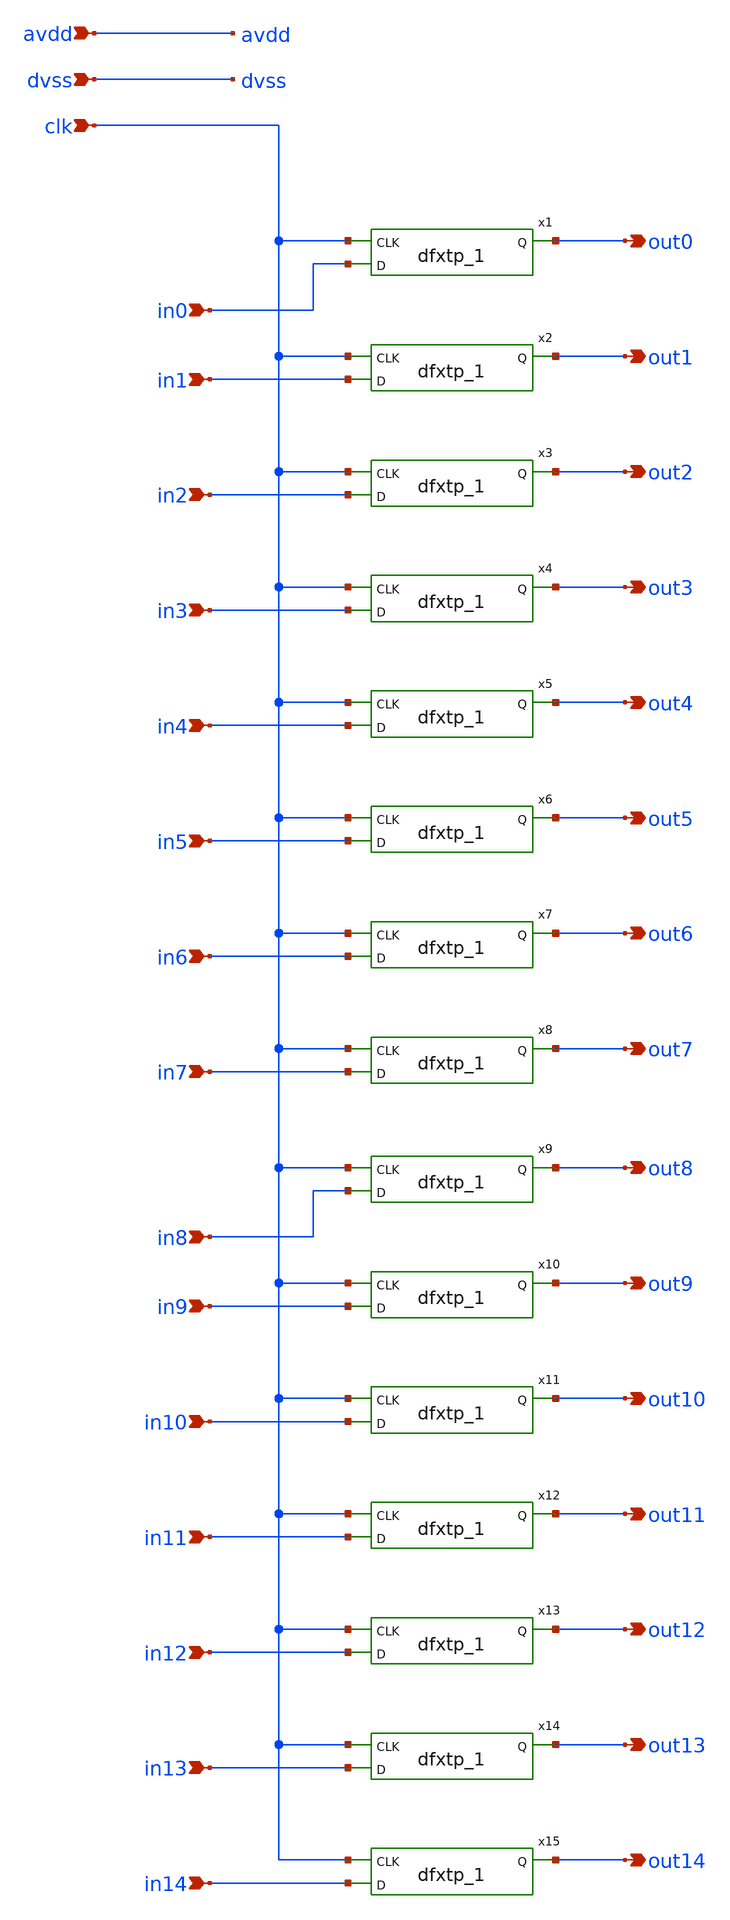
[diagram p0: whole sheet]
** sch_path: xschem/dff15ch.sch
**.subckt dff15ch out0 out1 out2 out3 out4 out5 out6 out7 in0 in1 in2 in3 in4 in5 in6 in7 out8 out9
*+ out10 out11 out12 out13 out14 in8 in9 in10 in11 in12 in13 in14 avdd dvss clk
*.opin out0
*.opin out1
*.opin out2
*.opin out3
*.opin out4
*.opin out5
*.opin out6
*.opin out7
*.ipin in0
*.ipin in1
*.ipin in2
*.ipin in3
*.ipin in4
*.ipin in5
*.ipin in6
*.ipin in7
*.opin out8
*.opin out9
*.opin out10
*.opin out11
*.opin out12
*.opin out13
*.opin out14
*.ipin in8
*.ipin in9
*.ipin in10
*.ipin in11
*.ipin in12
*.ipin in13
*.ipin in14
*.ipin avdd
*.ipin dvss
*.ipin clk
x1 clk in0 dvss dvss avdd avdd out0 sky130_fd_sc_hvl__dfxtp_1
x2 clk in1 dvss dvss avdd avdd out1 sky130_fd_sc_hvl__dfxtp_1
x3 clk in2 dvss dvss avdd avdd out2 sky130_fd_sc_hvl__dfxtp_1
x4 clk in3 dvss dvss avdd avdd out3 sky130_fd_sc_hvl__dfxtp_1
x5 clk in4 dvss dvss avdd avdd out4 sky130_fd_sc_hvl__dfxtp_1
x6 clk in5 dvss dvss avdd avdd out5 sky130_fd_sc_hvl__dfxtp_1
x7 clk in6 dvss dvss avdd avdd out6 sky130_fd_sc_hvl__dfxtp_1
x8 clk in7 dvss dvss avdd avdd out7 sky130_fd_sc_hvl__dfxtp_1
x9 clk in8 dvss dvss avdd avdd out8 sky130_fd_sc_hvl__dfxtp_1
x10 clk in9 dvss dvss avdd avdd out9 sky130_fd_sc_hvl__dfxtp_1
x11 clk in10 dvss dvss avdd avdd out10 sky130_fd_sc_hvl__dfxtp_1
x12 clk in11 dvss dvss avdd avdd out11 sky130_fd_sc_hvl__dfxtp_1
x13 clk in12 dvss dvss avdd avdd out12 sky130_fd_sc_hvl__dfxtp_1
x14 clk in13 dvss dvss avdd avdd out13 sky130_fd_sc_hvl__dfxtp_1
x15 clk in14 dvss dvss avdd avdd out14 sky130_fd_sc_hvl__dfxtp_1
**.ends
.end
